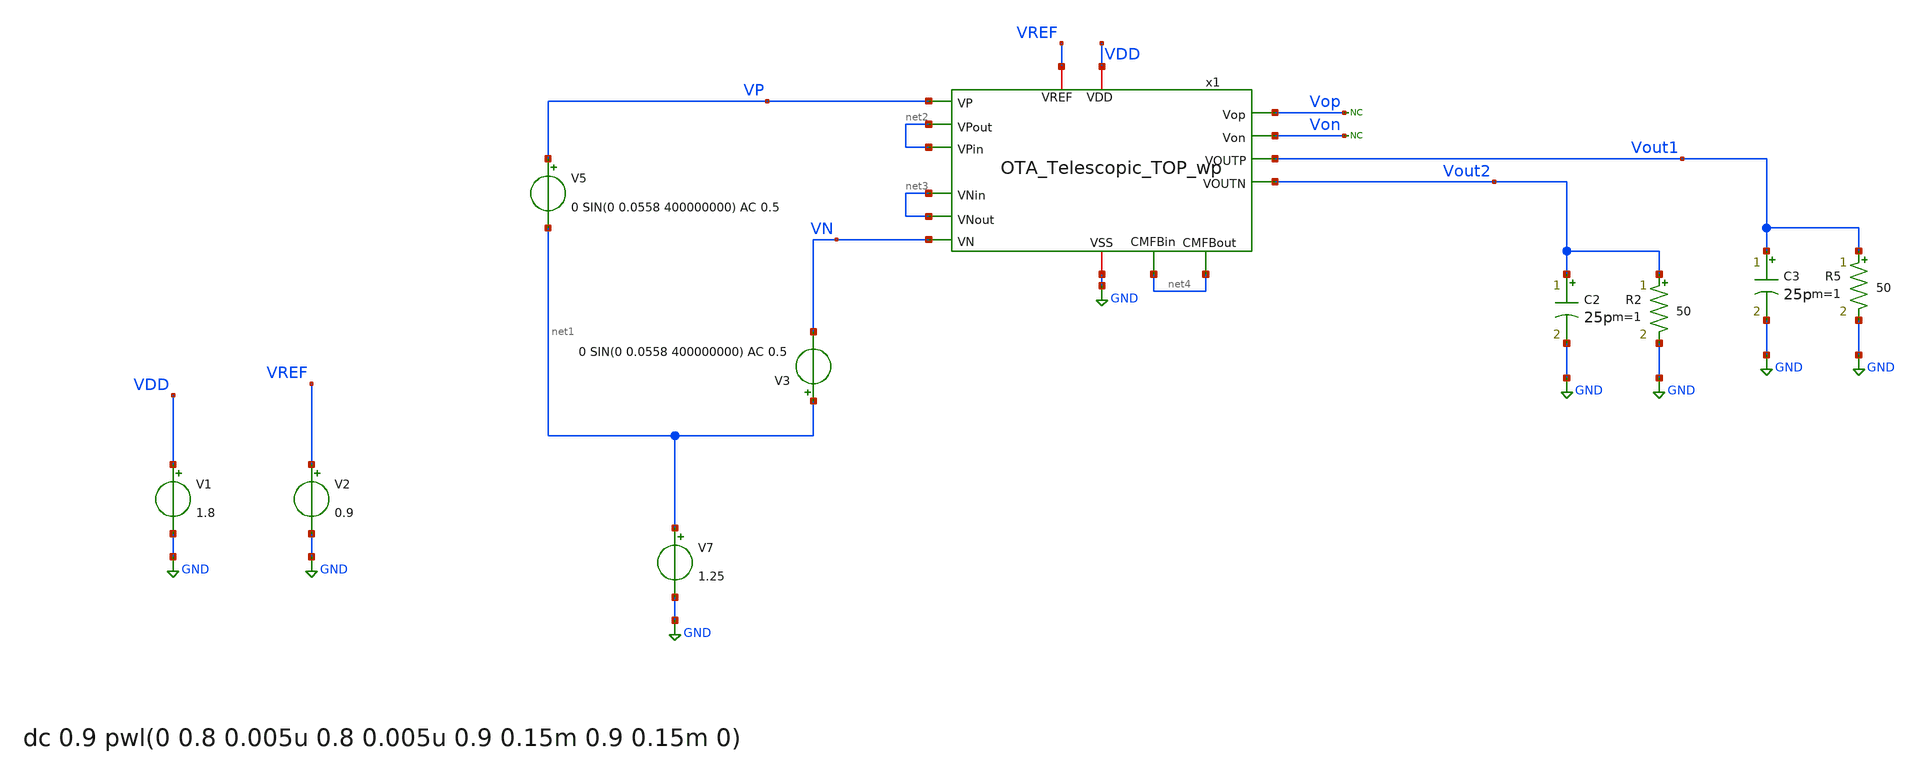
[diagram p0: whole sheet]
** sch_path: OTA_Telescopic_backup/OTA_Telescopic_NO_FLATTEN/Testbenchs/OTA_Telescopic_TOP_TB_CL.sch
**.subckt OTA_Telescopic_TOP_TB_CL
V7 net1 GND 1.25
V5 VP net1 0 SIN(0 0.0558 400000000) AC 0.5
V1 VDD GND 1.8
V2 VREF GND 0.9
V3 net1 VN 0 SIN(0 0.0558 400000000) AC 0.5
x1 VDD GND net2 net2 Vout1 VP VN Vout2 net3 net3 net4 VREF net4 Vop Von OTA_Telescopic_TOP_wp
C2 Vout2 GND 25p m=1
R2 Vout2 GND 50 m=1
C3 Vout1 GND 25p m=1
R5 Vout1 GND 50 m=1
* noconn Vop
* noconn Von
**** begin user architecture code

** opencircuitdesign pdks install
.lib cornerMOSlv.lib mos_tt
.lib cornerRES.lib res_typ
.lib cornerCAP.lib cap_typ
.temp 65



.control
save all
 set color0 = white

* AC simulation
ac dec 1000 1 1T
let Av = db(v(Vout1)-v(Vout2))
meas ac Ao FIND Av WHEN frequency=10
let ABW = Ao-3
meas ac BW WHEN Av=ABW
meas ac UGBW WHEN Av=0
let phase_vec = 180/pi*cph(v(Vout1)-v(Vout2))

* Phase margin (PM)
meas ac phase FIND phase_vec WHEN frequency=UGBW
let PM = phase+180
print PM

* Gain margin (GM)
meas ac freq180 FIND frequency WHEN phase_vec=-180
meas ac gain FIND Av WHEN frequency=freq180
let GM = 0-gain

print GM
plot Av
plot phase_vec

write AC_OL.raw
wrdata AvCL_ Av

*DC simulation

op
let vout_dc = v(Vout1)
print vout_dc
write OTA_Telescopic_TOP_TB_CL.raw

.endc


**** end user architecture code
**.ends
.GLOBAL GND
.end
